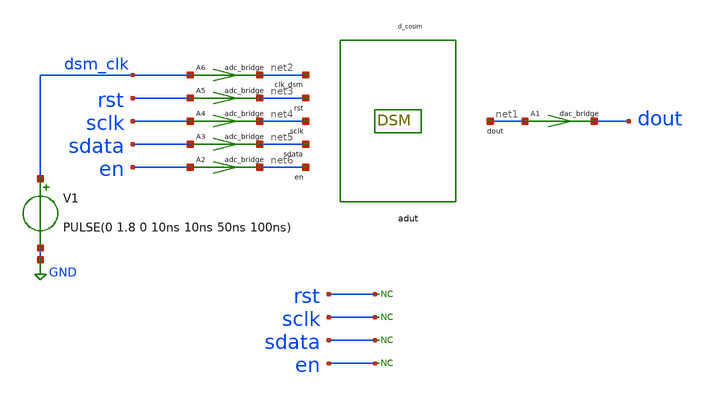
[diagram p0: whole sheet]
** sch_path: schematic/dsm/xschem/dsm_top_tb.sch
* Copyright (C) 1998-2024 Stefan Frederik Schippers
* This program is free software; you can redistribute it and/or modify
* it under the terms of the GNU General Public License as published by
* the Free Software Foundation; either version 2 of the License, or
* (at your option) any later version.
* This program is distributed in the hope that it will be useful,
* but WITHOUT ANY WARRANTY; without even the implied warranty of
* MERCHANTABILITY or FITNESS FOR A PARTICULAR PURPOSE.  See the
* GNU General Public License for more details.
* You should have received a copy of the GNU General Public License
* along with this program; if not, write to the Free Software
**.subckt dsm_top_tb
V1 dsm_clk GND PULSE(0 1.8 0 10ns 10ns 50ns 100ns)
A1 [ net1 ] [ dout ] dac1
.model dac1 dac_bridge out_low=0 out_high=1.2
A2 [ en ] [ net6 ] adc1
.model adc1 adc_bridge in_low=0.4 in_high=1.2
A3 [ sdata ] [ net5 ] adc1
.model adc1 adc_bridge in_low=0.4 in_high=1.2
A4 [ sclk ] [ net4 ] adc1
.model adc1 adc_bridge in_low=0.4 in_high=1.2
A5 [ rst ] [ net3 ] adc1
.model adc1 adc_bridge in_low=0.4 in_high=1.2
A6 [ dsm_clk ] [ net2 ] adc1
.model adc1 adc_bridge in_low=0.4 in_high=1.2
* noconn rst
* noconn sclk
* noconn sdata
* noconn en
adut [ net2 net3 net4 net5 net6 ] [ net1 ] null dut
.model dut d_cosim simulation=./../dsm_top.so
**** begin user architecture code



* ngspice commands
.save v(dout) v(sdata) v(sclk) v(en) v(rstn) v(dsm_clk) v(data_word0) v(data_word1) v(data_word2) v(data_word3) v(data_word4) v(data_word5) v(data_word6) v(data_word7) v(data_word8)
.control
  tran 0.5n 161702n
  remzerovec
  write test.raw
.endc

* to generate following file copy stimuli.test
* to the simulation directory and run simulation -> Utile Stimuli Editor (GUI),
* and press 'Translate'
.include stimuli_test.cir



**** end user architecture code
**.ends
.GLOBAL GND
.end
